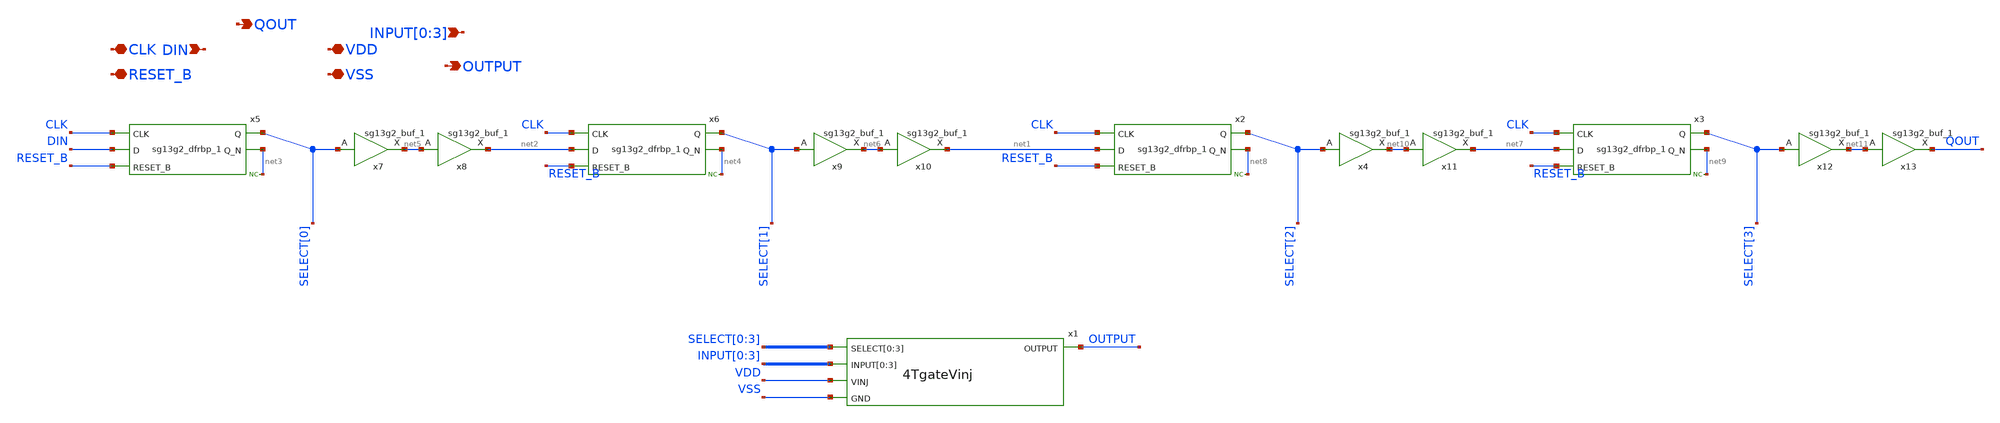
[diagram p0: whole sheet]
** sch_path: ihp130_cells/Scanner/Scanner.sch
* IHP-GmbH/IHP-Open-PDK/ihp-sg13g2/libs.tech/xschem/sg13g2_stdcells/sg13g2_buf_1.sch:
* Copyright 2023 IHP PDK Authors
* Licensed under the Apache License, Version 2.0 (the "License");
**.subckt Scanner CLK RESET_B DIN VDD VSS QOUT INPUT[0],INPUT[1],INPUT[2],INPUT[3] OUTPUT
*.iopin CLK
*.iopin RESET_B
*.ipin DIN
*.iopin VDD
*.iopin VSS
*.opin QOUT
*.ipin INPUT[0],INPUT[1],INPUT[2],INPUT[3]
*.opin OUTPUT
x5 SELECT[0] net3 CLK DIN RESET_B VDD VSS sg13g2_dfrbp_1
x6 SELECT[1] net4 CLK net2 RESET_B VDD VSS sg13g2_dfrbp_1
x7 net5 SELECT[0] VDD VSS sg13g2_buf_1
x8 net2 net5 VDD VSS sg13g2_buf_1
x9 net6 SELECT[1] VDD VSS sg13g2_buf_1
x10 net1 net6 VDD VSS sg13g2_buf_1
* noconn #net3
* noconn #net4
x1 SELECT[0] SELECT[1] SELECT[2] SELECT[3] OUTPUT INPUT[0] INPUT[1] INPUT[2] INPUT[3] VDD VSS
+ 4TgateVinj
x2 SELECT[2] net8 CLK net1 RESET_B VDD VSS sg13g2_dfrbp_1
x3 SELECT[3] net9 CLK net7 RESET_B VDD VSS sg13g2_dfrbp_1
x4 net10 SELECT[2] VDD VSS sg13g2_buf_1
x11 net7 net10 VDD VSS sg13g2_buf_1
x12 net11 SELECT[3] VDD VSS sg13g2_buf_1
x13 QOUT net11 VDD VSS sg13g2_buf_1
* noconn #net8
* noconn #net9
**.ends

* expanding   symbol:  sg13g2_stdcells/sg13g2_dfrbp_1.sym # of pins=5
** sym_path: sg13g2_stdcells/sg13g2_dfrbp_1.sym
** sch_path: sg13g2_stdcells/sg13g2_dfrbp_1.sch
.subckt sg13g2_dfrbp_1 Q Q_N CLK D RESET_B VDD VSS
*.ipin D
*.ipin RESET_B
*.ipin CLK
*.opin Q
*.opin Q_N
*.iopin VDD
*.iopin VSS
XM1 Db D net10 VSS sg13_lv_nmos w=420.00n l=130.00n ng=1 m=1 mm_ok=1
XM2 net10 RESET_B VSS VSS sg13_lv_nmos w=420.00n l=130.00n ng=1 m=1 mm_ok=1
XM3 net1 clkneg net9 VSS sg13_lv_nmos w=420.00n l=130.00n ng=1 m=1 mm_ok=1
XM4 net9 net1 VSS VSS sg13_lv_nmos w=420.00n l=130.00n ng=1 m=1 mm_ok=1
XM5 net1 net1 net5 VSS sg13_lv_nmos w=420.00n l=130.00n ng=1 m=1 mm_ok=1
XM6 net5 RESET_B VSS VSS sg13_lv_nmos w=420.00n l=130.00n ng=1 m=1 mm_ok=1
XM7 Q_N net1 VSS VSS sg13_lv_nmos w=740.00n l=130.00n ng=1 m=1 mm_ok=1
XM8 net2 net1 VSS VSS sg13_lv_nmos w=740.00n l=130.00n ng=1 m=1 mm_ok=1
XM9 Q net2 VSS VSS sg13_lv_nmos w=740.00n l=130.00n ng=1 m=1 mm_ok=1
XM10 clkneg CLK VSS VSS sg13_lv_nmos w=740.00n l=130.00n ng=1 m=1 mm_ok=1
XM11 clkpos clkneg VSS VSS sg13_lv_nmos w=740.00n l=130.00n ng=1 m=1 mm_ok=1
XM12 Db clkneg net3 VSS sg13_lv_nmos w=420.00n l=130.00n ng=1 m=1 mm_ok=1
XM13 net3 clkpos net8 VSS sg13_lv_nmos w=420.00n l=130.00n ng=1 m=1 mm_ok=1
XM14 net8 net3 net4 VSS sg13_lv_nmos w=420.00n l=130.00n ng=1 m=1 mm_ok=1
XM15 net4 RESET_B VSS VSS sg13_lv_nmos w=420.00n l=130.00n ng=1 m=1 mm_ok=1
XM16 net3 net3 VSS VSS sg13_lv_nmos w=740.00n l=130.00n ng=1 m=1 mm_ok=1
XM17 net3 clkpos net1 VSS sg13_lv_nmos w=740.00n l=130.00n ng=1 m=1 mm_ok=1
XM18 Db RESET_B VDD VDD sg13_lv_pmos w=420.00n l=130.00n ng=1 m=1 mm_ok=1
XM19 Db D VDD VDD sg13_lv_pmos w=420.00n l=130.00n ng=1 m=1 mm_ok=1
XM20 net7 net1 VDD VDD sg13_lv_pmos w=420.00n l=130.00n ng=1 m=1 mm_ok=1
XM21 net1 clkpos net7 VDD sg13_lv_pmos w=420.00n l=130.00n ng=1 m=1 mm_ok=1
XM22 net1 net1 VDD VDD sg13_lv_pmos w=420.00n l=130.00n ng=1 m=1 mm_ok=1
XM23 net1 RESET_B VDD VDD sg13_lv_pmos w=420.00n l=130.00n ng=1 m=1 mm_ok=1
XM24 Q_N net1 VDD VDD sg13_lv_pmos w=1.12u l=130.00n ng=1 m=1 mm_ok=1
XM25 net2 net1 VDD VDD sg13_lv_pmos w=1.12u l=130.00n ng=1 m=1 mm_ok=1
XM26 Q net2 VDD VDD sg13_lv_pmos w=1.12u l=130.00n ng=1 m=1 mm_ok=1
XM27 clkneg CLK VDD VDD sg13_lv_pmos w=1.12u l=130.00n ng=1 m=1 mm_ok=1
XM28 clkpos clkneg VDD VDD sg13_lv_pmos w=1.12u l=130.00n ng=1 m=1 mm_ok=1
XM29 Db clkpos net3 VDD sg13_lv_pmos w=420.00n l=130.00n ng=1 m=1 mm_ok=1
XM30 net6 net3 VDD VDD sg13_lv_pmos w=420.00n l=130.00n ng=1 m=1 mm_ok=1
XM31 net3 clkneg net6 VDD sg13_lv_pmos w=420.00n l=130.00n ng=1 m=1 mm_ok=1
XM32 net3 RESET_B VDD VDD sg13_lv_pmos w=420.00n l=130.00n ng=1 m=1 mm_ok=1
XM33 net3 net3 VDD VDD sg13_lv_pmos w=1.000u l=130.00n ng=1 m=1 mm_ok=1
XM34 net3 clkneg net1 VDD sg13_lv_pmos w=1.000u l=130.00n ng=1 m=1 mm_ok=1
.ends


* expanding   symbol:  sg13g2_stdcells/sg13g2_buf_1.sym # of pins=2
** sym_path: sg13g2_stdcells/sg13g2_buf_1.sym
** sch_path: sg13g2_stdcells/sg13g2_buf_1.sch
.subckt sg13g2_buf_1 X A VDD VSS
*.ipin A
*.opin X
*.iopin VDD
*.iopin VSS
XM1 net1 A VSS VSS sg13_lv_nmos w=550.00n l=130.00n ng=1 m=1 mm_ok=1
XM2 X net1 VSS VSS sg13_lv_nmos w=740.00n l=130.00n ng=1 m=1 mm_ok=1
XM3 net1 A VDD VDD sg13_lv_pmos w=840.00n l=130.00n ng=1 m=1 mm_ok=1
XM4 X net1 VDD VDD sg13_lv_pmos w=1.12u l=130.00n ng=1 m=1 mm_ok=1
.ends


* expanding   symbol:  4TgateVinj/4TgateVinj.sym # of pins=5
** sym_path: ihp130_cells/4TgateVinj/4TgateVinj.sym
** sch_path: ihp130_cells/4TgateVinj/4TgateVinj.sch
.subckt 4TgateVinj SELECT[0] SELECT[1] SELECT[2] SELECT[3] OUTPUT INPUT[0] INPUT[1] INPUT[2]
+ INPUT[3] VINJ GND
*.ipin SELECT[0],SELECT[1],SELECT[2],SELECT[3]
*.ipin INPUT[0],INPUT[1],INPUT[2],INPUT[3]
*.ipin VINJ
*.ipin GND
*.opin OUTPUT
x1 SELECT[0] INPUT[0] VINJ GND OUTPUT ihp130_TgateVinj02
x2 SELECT[1] INPUT[1] VINJ GND OUTPUT ihp130_TgateVinj02
x3 SELECT[2] INPUT[2] VINJ GND OUTPUT ihp130_TgateVinj02
x4 SELECT[3] INPUT[3] VINJ GND OUTPUT ihp130_TgateVinj02
.ends


* expanding   symbol:  TgateVinj02/ihp130_TgateVinj02.sym # of pins=5
** sym_path: ihp130_cells/TgateVinj02/ihp130_TgateVinj02.sym
** sch_path: ihp130_cells/TgateVinj02/ihp130_TgateVinj02.sch
.subckt ihp130_TgateVinj02 SELECT INPUT VINJ GND OUTPUT
*.ipin SELECT
*.ipin INPUT
*.ipin VINJ
*.ipin GND
*.opin OUTPUT
XM1 Selb SELECT VINJ VINJ sg13_hv_pmos w=0.42u l=0.5u ng=1 m=1 mm_ok=1
XM2 Selb SELECT GND GND sg13_hv_nmos w=0.42u l=0.5u ng=1 m=1 mm_ok=1
XM3 INPUT Selb OUTPUT VINJ sg13_hv_pmos w=0.42u l=0.5u ng=1 m=1 mm_ok=1
XM4 INPUT SELECT OUTPUT GND sg13_hv_nmos w=0.42u l=0.5u ng=1 m=1 mm_ok=1
.ends

.end
